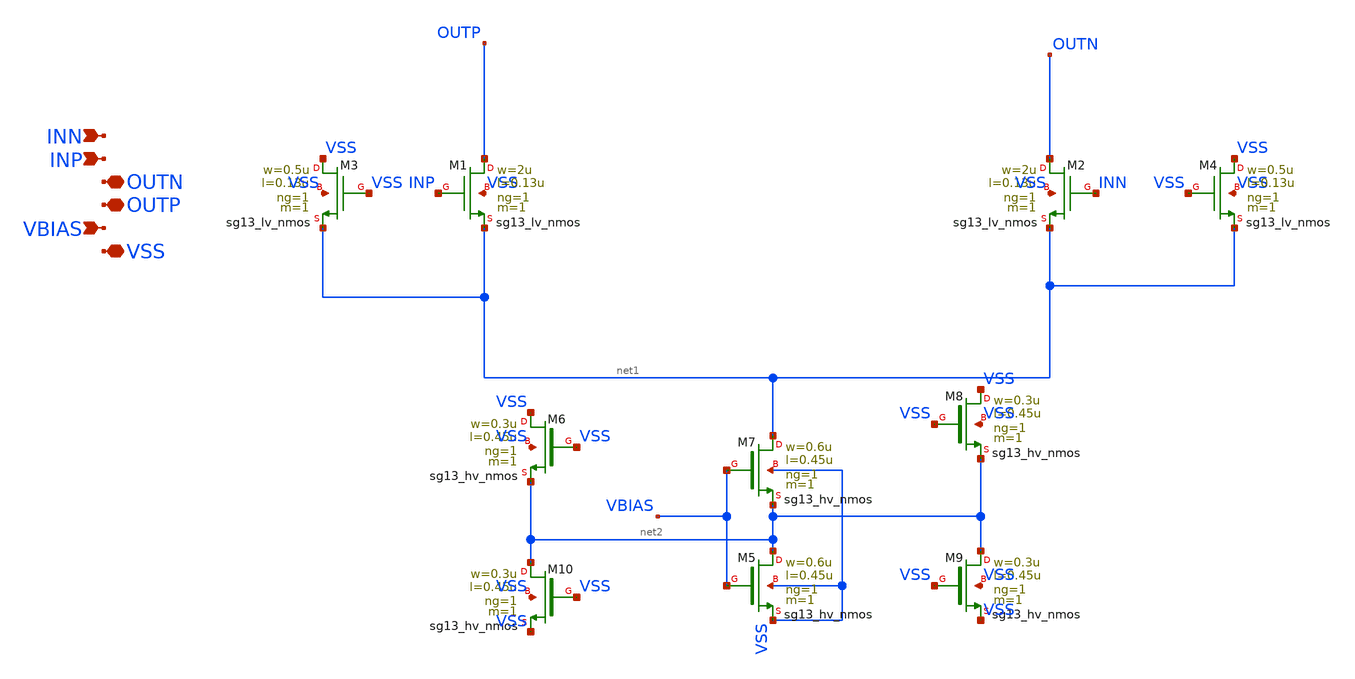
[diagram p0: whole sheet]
** sch_path: dependencies/DAC/DAC-main/schematic/xschem/CS_Switch_2x.sch
**.subckt CS_Switch_2x VSS VBIAS OUTP OUTN INP INN
*.iopin VSS
*.ipin VBIAS
*.iopin OUTP
*.iopin OUTN
*.ipin INP
*.ipin INN
XM7 net1 VBIAS net2 VSS sg13_hv_nmos w=0.6u l=0.45u ng=1 m=1 mm_ok=1
XM5 net2 VBIAS VSS VSS sg13_hv_nmos w=0.6u l=0.45u ng=1 m=1 mm_ok=1
XM1 OUTP INP net1 VSS sg13_lv_nmos w=2u l=0.13u ng=1 m=1 mm_ok=1
XM2 OUTN INN net1 VSS sg13_lv_nmos w=2u l=0.13u ng=1 m=1 mm_ok=1
XM3 VSS VSS net1 VSS sg13_lv_nmos w=0.5u l=0.13u ng=1 m=1 mm_ok=1
XM6 VSS VSS net2 VSS sg13_hv_nmos w=0.3u l=0.45u ng=1 m=1 mm_ok=1
XM8 VSS VSS net2 VSS sg13_hv_nmos w=0.3u l=0.45u ng=1 m=1 mm_ok=1
XM9 net2 VSS VSS VSS sg13_hv_nmos w=0.3u l=0.45u ng=1 m=1 mm_ok=1
XM10 net2 VSS VSS VSS sg13_hv_nmos w=0.3u l=0.45u ng=1 m=1 mm_ok=1
XM4 VSS VSS net1 VSS sg13_lv_nmos w=0.5u l=0.13u ng=1 m=1 mm_ok=1
**.ends
.end
